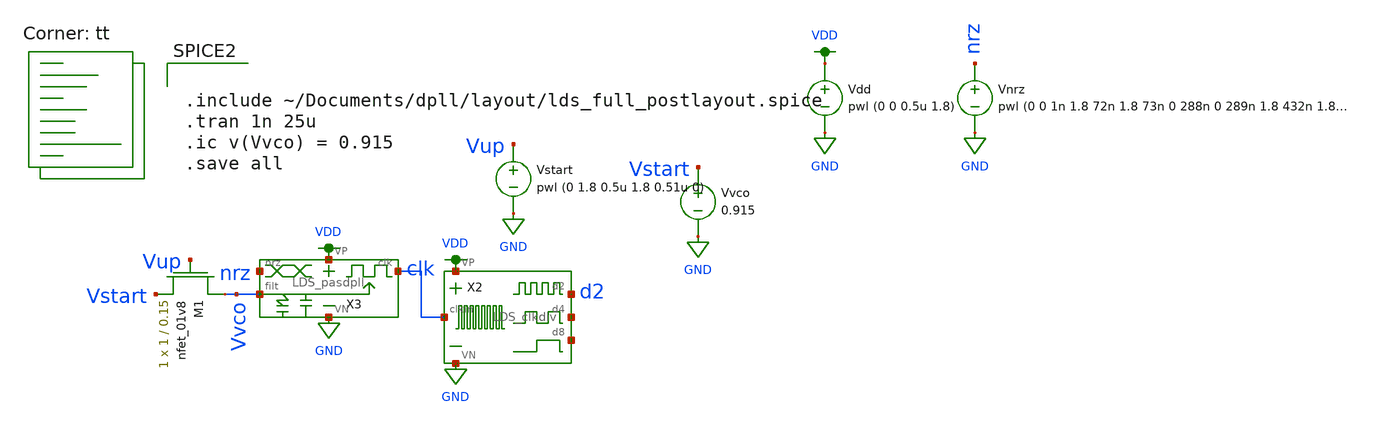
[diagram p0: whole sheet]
** sch_path: LDS/test_full_w_passive.sch
**.subckt test_full_w_passive
Vdd VDD GND pwl (0 0 0.5u 1.8)
Vnrz nrz GND pwl (0 0 1n 1.8 72n 1.8 73n 0 288n 0 289n 1.8 432n 1.8 433n 0 504n 0) R=0 td=1u
Vvco Vstart GND 0.915
XM1 Vvco Vup Vstart GND sky130_fd_pr__nfet_01v8 L=0.15 W=1 nf=1 ad='int((nf+1)/2) * W/nf * 0.29' as='int((nf+2)/2) * W/nf * 0.29'
+ pd='2*int((nf+1)/2) * (W/nf + 0.29)' ps='2*int((nf+2)/2) * (W/nf + 0.29)' nrd='0.29 / W' nrs='0.29 / W'
+ sa=0 sb=0 sd=0 mult=1 m=1
Vstart Vup GND pwl (0 1.8 0.5u 1.8 0.51u 0)
X2 VDD GND clk d2 net1 net2 LDS_clkdiv
X3 VDD GND Vvco nrz clk LDS_pasdpll
**** begin user architecture code
.lib $::SKYWATER_MODELS/sky130.lib.spice tt


.include ~/Documents/dpll/layout/lds_full_postlayout.spice
.tran 1n 25u
.ic v(Vvco) = 0.915
.save all


**** end user architecture code
**.ends
.GLOBAL VDD
.GLOBAL GND
.end
